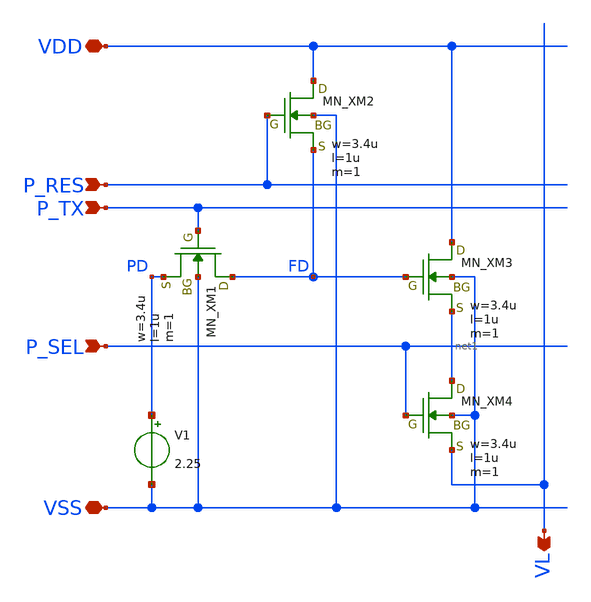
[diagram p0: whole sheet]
** sch_path: member_project/imager/YuMaehashi/design/pix_unit_test3.sch
**.subckt pix_unit_test3 P_RES VDD VL VSS P_TX P_SEL
*.ipin P_RES
*.iopin VDD
*.opin VL
*.iopin VSS
*.ipin P_TX
*.ipin P_SEL
XXM1 FD P_TX PD VSS NMOS w=3.4u l=1u nrd=0 nrs=0 m=1
XXM2 VDD P_RES FD VSS NMOS w=3.4u l=1u nrd=0 nrs=0 m=1
XXM3 VDD FD net1 VSS NMOS w=3.4u l=1u nrd=0 nrs=0 m=1
XXM4 net1 P_SEL VL VSS NMOS w=3.4u l=1u nrd=0 nrs=0 m=1
V1 PD VSS 2.25
**.ends
.end
